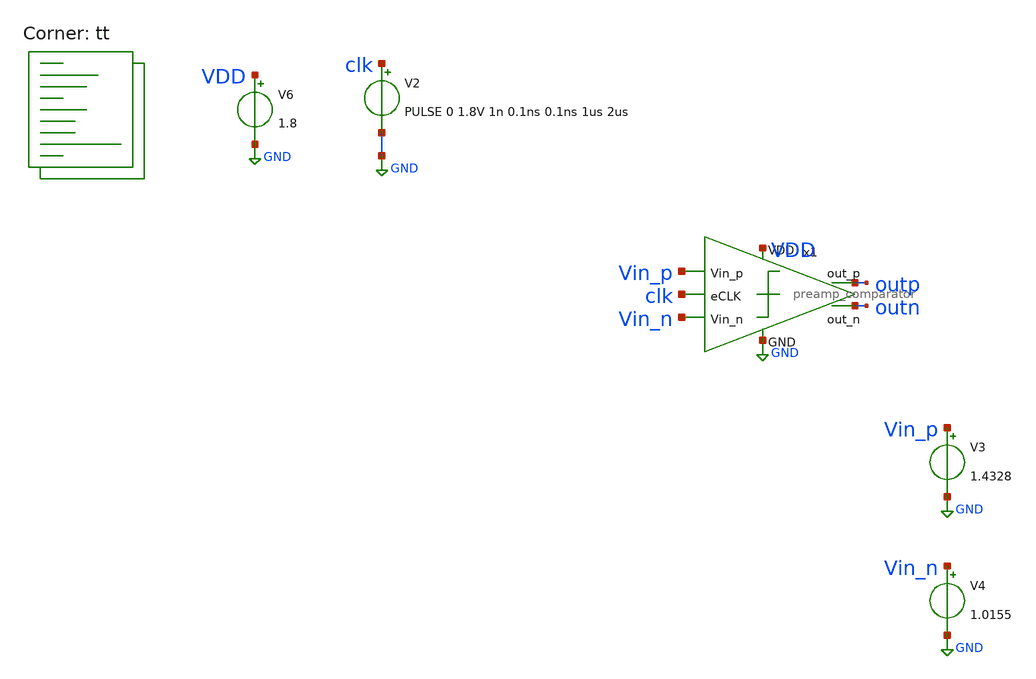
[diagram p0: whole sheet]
** sch_path: xschem/comparator/preamp_comparator_test.sch
**.subckt preamp_comparator_test
x1 VDD GND clk Vin_p Vin_n outp outn preamp_comparator
V6 VDD GND 1.8
V2 clk GND PULSE 0 1.8V 1n 0.1ns 0.1ns 1us 2us
V3 Vin_p GND 1.4328
V4 Vin_n GND 1.0155
**** begin user architecture code
.lib $::SKYWATER_MODELS/sky130.lib.spice tt
 *.lib $::SKYWATER_MODELS/sky130.lib.spice tt
.include $::SKYWATER_STDCELLS/sky130_fd_sc_hd.spice




.control
tran 0.1u 10u uic

write comp_test.raw
.endc




**** end user architecture code
**.ends

* expanding   symbol:  preamp_comparator.sym # of pins=7
** sym_path: xschem/comparator/preamp_comparator.sym
** sch_path: xschem/comparator/preamp_comparator.sch
.subckt preamp_comparator VDD GND eCLK Vin_p Vin_n out_p out_n
*.ipin eCLK
*.ipin Vin_p
*.ipin Vin_n
*.opin out_n
*.opin out_p
*.iopin VDD
*.iopin GND
XM10 Pre_amp_p CLK_n VDD VDD sky130_fd_pr__pfet_01v8 L=0.15 W=20 nf=1 ad='int((nf+1)/2) * W/nf * 0.29'
+ as='int((nf+2)/2) * W/nf * 0.29' pd='2*int((nf+1)/2) * (W/nf + 0.29)' ps='2*int((nf+2)/2) * (W/nf + 0.29)'
+ nrd='0.29 / W' nrs='0.29 / W' sa=0 sb=0 sd=0 mult=1 m=1
XM1 Pre_amp_n CLK_n VDD VDD sky130_fd_pr__pfet_01v8 L=0.15 W=20 nf=1 ad='int((nf+1)/2) * W/nf * 0.29'
+ as='int((nf+2)/2) * W/nf * 0.29' pd='2*int((nf+1)/2) * (W/nf + 0.29)' ps='2*int((nf+2)/2) * (W/nf + 0.29)'
+ nrd='0.29 / W' nrs='0.29 / W' sa=0 sb=0 sd=0 mult=1 m=1
XM4 net1 CLK GND GND sky130_fd_pr__nfet_01v8 L=0.15 W=50 nf=1 ad='int((nf+1)/2) * W/nf * 0.29' as='int((nf+2)/2) * W/nf * 0.29'
+ pd='2*int((nf+1)/2) * (W/nf + 0.29)' ps='2*int((nf+2)/2) * (W/nf + 0.29)' nrd='0.29 / W' nrs='0.29 / W'
+ sa=0 sb=0 sd=0 mult=1 m=1
XM5 net2 net5 VDD VDD sky130_fd_pr__pfet_01v8 L=0.15 W=1.605 nf=1 ad='int((nf+1)/2) * W/nf * 0.29' as='int((nf+2)/2) * W/nf * 0.29'
+ pd='2*int((nf+1)/2) * (W/nf + 0.29)' ps='2*int((nf+2)/2) * (W/nf + 0.29)' nrd='0.29 / W' nrs='0.29 / W'
+ sa=0 sb=0 sd=0 mult=4 m=4
XM6 net3 net4 VDD VDD sky130_fd_pr__pfet_01v8 L=0.15 W=1.605 nf=1 ad='int((nf+1)/2) * W/nf * 0.29' as='int((nf+2)/2) * W/nf * 0.29'
+ pd='2*int((nf+1)/2) * (W/nf + 0.29)' ps='2*int((nf+2)/2) * (W/nf + 0.29)' nrd='0.29 / W' nrs='0.29 / W'
+ sa=0 sb=0 sd=0 mult=4 m=4
XM7 net4 Pre_amp_n net2 VDD sky130_fd_pr__pfet_01v8 L=0.15 W=1.605 nf=1 ad='int((nf+1)/2) * W/nf * 0.29'
+ as='int((nf+2)/2) * W/nf * 0.29' pd='2*int((nf+1)/2) * (W/nf + 0.29)' ps='2*int((nf+2)/2) * (W/nf + 0.29)'
+ nrd='0.29 / W' nrs='0.29 / W' sa=0 sb=0 sd=0 mult=8 m=8
XM8 net5 Pre_amp_p net3 VDD sky130_fd_pr__pfet_01v8 L=0.15 W=1.605 nf=1 ad='int((nf+1)/2) * W/nf * 0.29'
+ as='int((nf+2)/2) * W/nf * 0.29' pd='2*int((nf+1)/2) * (W/nf + 0.29)' ps='2*int((nf+2)/2) * (W/nf + 0.29)'
+ nrd='0.29 / W' nrs='0.29 / W' sa=0 sb=0 sd=0 mult=8 m=8
XM9 net4 net5 GND GND sky130_fd_pr__nfet_01v8 L=0.15 W=0.91 nf=1 ad='int((nf+1)/2) * W/nf * 0.29' as='int((nf+2)/2) * W/nf * 0.29'
+ pd='2*int((nf+1)/2) * (W/nf + 0.29)' ps='2*int((nf+2)/2) * (W/nf + 0.29)' nrd='0.29 / W' nrs='0.29 / W'
+ sa=0 sb=0 sd=0 mult=4 m=4
XM11 net5 net4 GND GND sky130_fd_pr__nfet_01v8 L=0.15 W=0.91 nf=1 ad='int((nf+1)/2) * W/nf * 0.29' as='int((nf+2)/2) * W/nf * 0.29'
+ pd='2*int((nf+1)/2) * (W/nf + 0.29)' ps='2*int((nf+2)/2) * (W/nf + 0.29)' nrd='0.29 / W' nrs='0.29 / W'
+ sa=0 sb=0 sd=0 mult=4 m=4
XM12 net4 CLK_latch_n GND GND sky130_fd_pr__nfet_01v8 L=0.15 W=0.91 nf=1 ad='int((nf+1)/2) * W/nf * 0.29'
+ as='int((nf+2)/2) * W/nf * 0.29' pd='2*int((nf+1)/2) * (W/nf + 0.29)' ps='2*int((nf+2)/2) * (W/nf + 0.29)'
+ nrd='0.29 / W' nrs='0.29 / W' sa=0 sb=0 sd=0 mult=4 m=4
XM13 net5 CLK_latch_n GND GND sky130_fd_pr__nfet_01v8 L=0.15 W=0.91 nf=1 ad='int((nf+1)/2) * W/nf * 0.29'
+ as='int((nf+2)/2) * W/nf * 0.29' pd='2*int((nf+1)/2) * (W/nf + 0.29)' ps='2*int((nf+2)/2) * (W/nf + 0.29)'
+ nrd='0.29 / W' nrs='0.29 / W' sa=0 sb=0 sd=0 mult=4 m=4
x2 CLK_n GND GND VDD VDD net6 sky130_fd_sc_hd__clkdlybuf4s15_1
x6 eCLK GND GND VDD VDD net9 sky130_fd_sc_hd__buf_1
x7 net10 GND GND VDD VDD CLK sky130_fd_sc_hd__buf_4
x12 net12 GND GND VDD VDD out_n sky130_fd_sc_hd__buf_8
x16 CLK GND GND VDD VDD CLK_n sky130_fd_sc_hd__inv_2
x1 net7 GND GND VDD VDD net8 sky130_fd_sc_hd__clkdlybuf4s50_2
x4 net8 GND GND VDD VDD CLK_latch_n sky130_fd_sc_hd__buf_2
x3 net6 GND GND VDD VDD net7 sky130_fd_sc_hd__clkdlybuf4s15_1
x9 net9 GND GND VDD VDD net10 sky130_fd_sc_hd__buf_2
x5 net5 GND GND VDD VDD net11 sky130_fd_sc_hd__buf_1
x8 net11 GND GND VDD VDD net12 sky130_fd_sc_hd__buf_4
x10 net4 GND GND VDD VDD net14 sky130_fd_sc_hd__buf_1
x11 net14 GND GND VDD VDD net13 sky130_fd_sc_hd__buf_4
x13 net13 GND GND VDD VDD out_p sky130_fd_sc_hd__buf_8
XM14 Pre_amp_n Vin_p net1 GND sky130_fd_pr__nfet_01v8_lvt L=0.15 W=40 nf=1 ad='int((nf+1)/2) * W/nf * 0.29'
+ as='int((nf+2)/2) * W/nf * 0.29' pd='2*int((nf+1)/2) * (W/nf + 0.29)' ps='2*int((nf+2)/2) * (W/nf + 0.29)'
+ nrd='0.29 / W' nrs='0.29 / W' sa=0 sb=0 sd=0 mult=1 m=1
XM3 Pre_amp_p Vin_n net1 GND sky130_fd_pr__nfet_01v8_lvt L=0.15 W=40 nf=1 ad='int((nf+1)/2) * W/nf * 0.29'
+ as='int((nf+2)/2) * W/nf * 0.29' pd='2*int((nf+1)/2) * (W/nf + 0.29)' ps='2*int((nf+2)/2) * (W/nf + 0.29)'
+ nrd='0.29 / W' nrs='0.29 / W' sa=0 sb=0 sd=0 mult=1 m=1
.ends

.GLOBAL GND
.end
